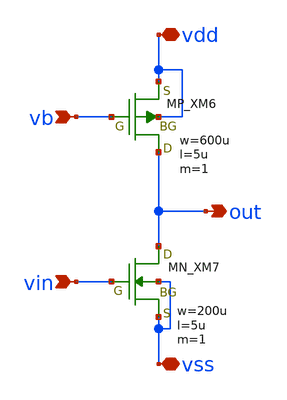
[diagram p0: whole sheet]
** sch_path: member_project/OPAMP/kano/sch_tb/cs.sch
**.subckt cs vb vin out vss vdd
*.ipin vb
*.ipin vin
*.opin out
*.iopin vss
*.iopin vdd
XM6 out vb vdd vdd PMOS w=600u l=5u as=0 ad=0 ps=0 pd=0 nrd=0 nrs=0 m=1
XM7 out vin vss vss NMOS w=200u l=5u as=0 ad=0 ps=0 pd=0 nrd=0 nrs=0 m=1
**.ends
.end
